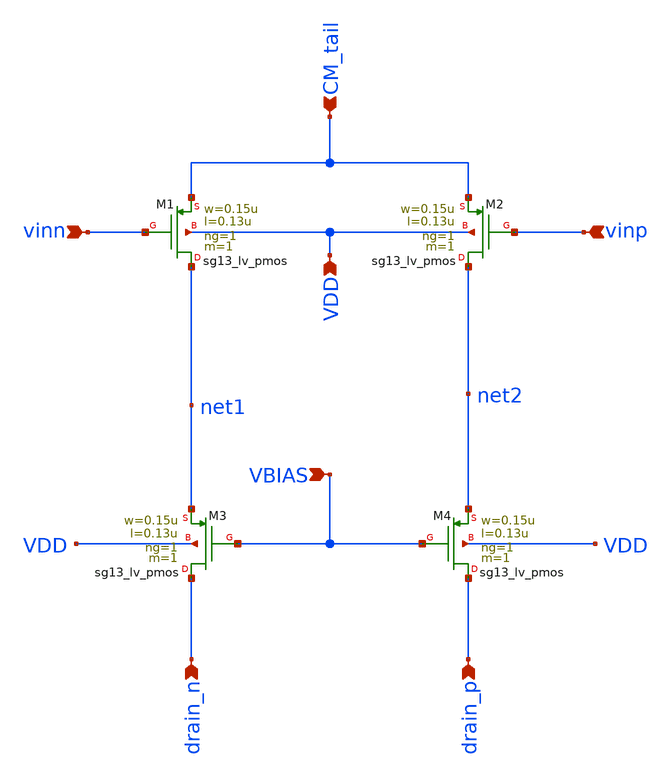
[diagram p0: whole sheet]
** sch_path: analog-db/templates/miscellaneous/diff_pair_improved_pmos.sch
* Copyright 2026 MacAnalog Research Group
**.subckt diff_pair_improved_pmos vinp vinn CM_tail drain_n drain_p VDD VBIAS
*.ipin vinp
*.ipin vinn
*.ipin CM_tail
*.ipin drain_n
*.ipin drain_p
*.ipin VDD
*.ipin VBIAS
XM1 net1 vinn CM_tail VDD sg13_lv_pmos w=0.15u l=0.13u ng=1 m=1 mm_ok=1
XM2 net2 vinp CM_tail VDD sg13_lv_pmos w=0.15u l=0.13u ng=1 m=1 mm_ok=1
XM3 drain_n VBIAS net1 VDD sg13_lv_pmos w=0.15u l=0.13u ng=1 m=1 mm_ok=1
XM4 drain_p VBIAS net2 VDD sg13_lv_pmos w=0.15u l=0.13u ng=1 m=1 mm_ok=1
**.ends
.end
